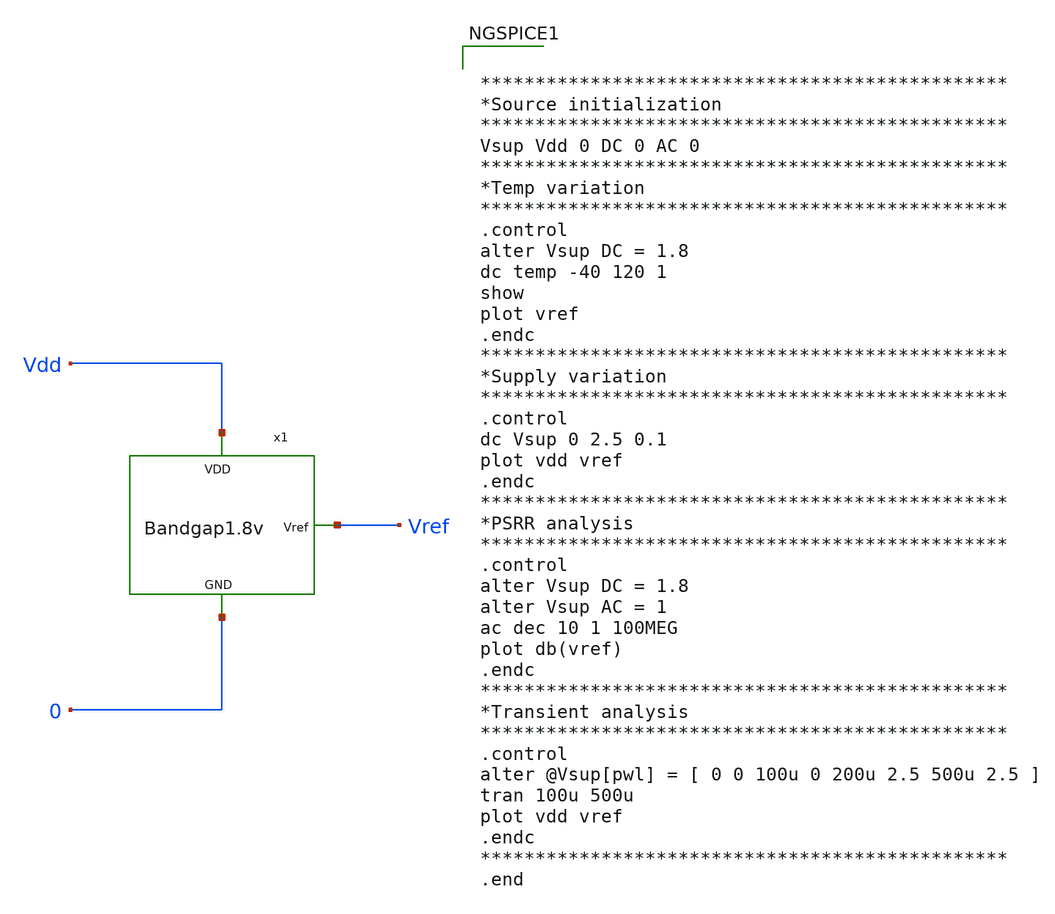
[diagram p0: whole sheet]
** sch_path: Analog_Blocks/Bandgap/Testbench/Bandgap1.8v_TB.sch
**.subckt Bandgap1.8v_TB
x1 Vref Vdd 0 Bandgap1.8v
**** begin user architecture code

.include $::SKYWATER_MODELS/cells/nfet_01v8/sky130_fd_pr__nfet_01v8__tt.corner.spice
.include $::SKYWATER_MODELS/cells/nfet_01v8_lvt/sky130_fd_pr__nfet_01v8_lvt__tt.corner.spice
.include $::SKYWATER_MODELS/cells/pfet_01v8/sky130_fd_pr__pfet_01v8__tt.corner.spice
.include $::SKYWATER_MODELS/cells/nfet_03v3_nvt/sky130_fd_pr__nfet_03v3_nvt__tt.corner.spice
.include $::SKYWATER_MODELS/cells/nfet_05v0_nvt/sky130_fd_pr__nfet_05v0_nvt__tt.corner.spice
.include $::SKYWATER_MODELS/cells/esd_nfet_01v8/sky130_fd_pr__esd_nfet_01v8__tt.corner.spice
.include $::SKYWATER_MODELS/cells/pfet_01v8_lvt/sky130_fd_pr__pfet_01v8_lvt__tt.corner.spice
.include $::SKYWATER_MODELS/cells/pfet_01v8_hvt/sky130_fd_pr__pfet_01v8_hvt__tt.corner.spice
.include $::SKYWATER_MODELS/cells/esd_pfet_g5v0d10v5/sky130_fd_pr__esd_pfet_g5v0d10v5__tt.corner.spice
.include $::SKYWATER_MODELS/cells/pfet_g5v0d10v5/sky130_fd_pr__pfet_g5v0d10v5__tt.corner.spice
.include $::SKYWATER_MODELS/cells/pfet_g5v0d16v0/sky130_fd_pr__pfet_g5v0d16v0__tt.corner.spice
.include $::SKYWATER_MODELS/cells/nfet_g5v0d10v5/sky130_fd_pr__nfet_g5v0d10v5__tt.corner.spice
.include $::SKYWATER_MODELS/cells/nfet_g5v0d16v0/sky130_fd_pr__nfet_g5v0d16v0__tt_discrete.corner.spice
.include $::SKYWATER_MODELS/cells/esd_nfet_g5v0d10v5/sky130_fd_pr__esd_nfet_g5v0d10v5__tt.corner.spice
.include $::SKYWATER_MODELS/models/corners/tt/nonfet.spice
* Mismatch parameters
.include $::SKYWATER_MODELS/cells/nfet_01v8/sky130_fd_pr__nfet_01v8__mismatch.corner.spice
.include $::SKYWATER_MODELS/cells/pfet_01v8/sky130_fd_pr__pfet_01v8__mismatch.corner.spice
.include $::SKYWATER_MODELS/cells/nfet_01v8_lvt/sky130_fd_pr__nfet_01v8_lvt__mismatch.corner.spice
.include $::SKYWATER_MODELS/cells/pfet_01v8_lvt/sky130_fd_pr__pfet_01v8_lvt__mismatch.corner.spice
.include $::SKYWATER_MODELS/cells/pfet_01v8_hvt/sky130_fd_pr__pfet_01v8_hvt__mismatch.corner.spice
.include $::SKYWATER_MODELS/cells/nfet_g5v0d10v5/sky130_fd_pr__nfet_g5v0d10v5__mismatch.corner.spice
.include $::SKYWATER_MODELS/cells/pfet_g5v0d10v5/sky130_fd_pr__pfet_g5v0d10v5__mismatch.corner.spice
.include $::SKYWATER_MODELS/cells/nfet_05v0_nvt/sky130_fd_pr__nfet_05v0_nvt__mismatch.corner.spice
.include $::SKYWATER_MODELS/cells/nfet_03v3_nvt/sky130_fd_pr__nfet_03v3_nvt__mismatch.corner.spice
* Resistor$::SKYWATER_MODELS/Capacitor
.include $::SKYWATER_MODELS/models/r+c/res_typical__cap_typical.spice
.include $::SKYWATER_MODELS/models/r+c/res_typical__cap_typical__lin.spice
* Special cells
.include $::SKYWATER_MODELS/models/corners/tt/specialized_cells.spice
* All models
.include $::SKYWATER_MODELS/models/all.spice
* Corner
.include $::SKYWATER_MODELS/models/corners/tt/rf.spice



************************************************
*Source initialization
************************************************
Vsup Vdd 0 DC 0 AC 0
************************************************
*Temp variation
************************************************
.control
alter Vsup DC = 1.8
dc temp -40 120 1
show
plot vref
.endc
************************************************
*Supply variation
************************************************
.control
dc Vsup 0 2.5 0.1
plot vdd vref
.endc
************************************************
*PSRR analysis
************************************************
.control
alter Vsup DC = 1.8
alter Vsup AC = 1
ac dec 10 1 100MEG
plot db(vref)
.endc
************************************************
*Transient analysis
************************************************
.control
alter @Vsup[pwl] = [ 0 0 100u 0 200u 2.5 500u 2.5 ]
tran 100u 500u
plot vdd vref
.endc
************************************************
.end


**** end user architecture code
**.ends
.end
